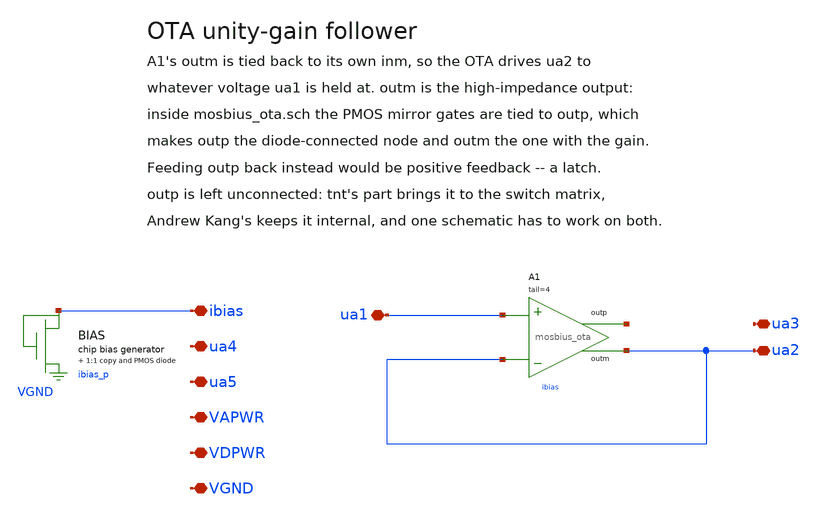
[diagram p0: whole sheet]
** sch_path: examples/otabuf/otabuf.sch
**.subckt otabuf ibias ua1 ua2 ua3 ua4 ua5 VAPWR VDPWR VGND
*.iopin ibias
*.iopin ua1
*.iopin ua2
*.iopin ua3
*.iopin ua4
*.iopin ua5
*.iopin VAPWR
*.iopin VDPWR
*.iopin VGND
XA1 ua1 ua2 net1 ua2 ibias VGND VAPWR mosbius_ota tail=4
XBIAS ibias ibias_p VGND VAPWR mosbius_bias
**.ends
.end
